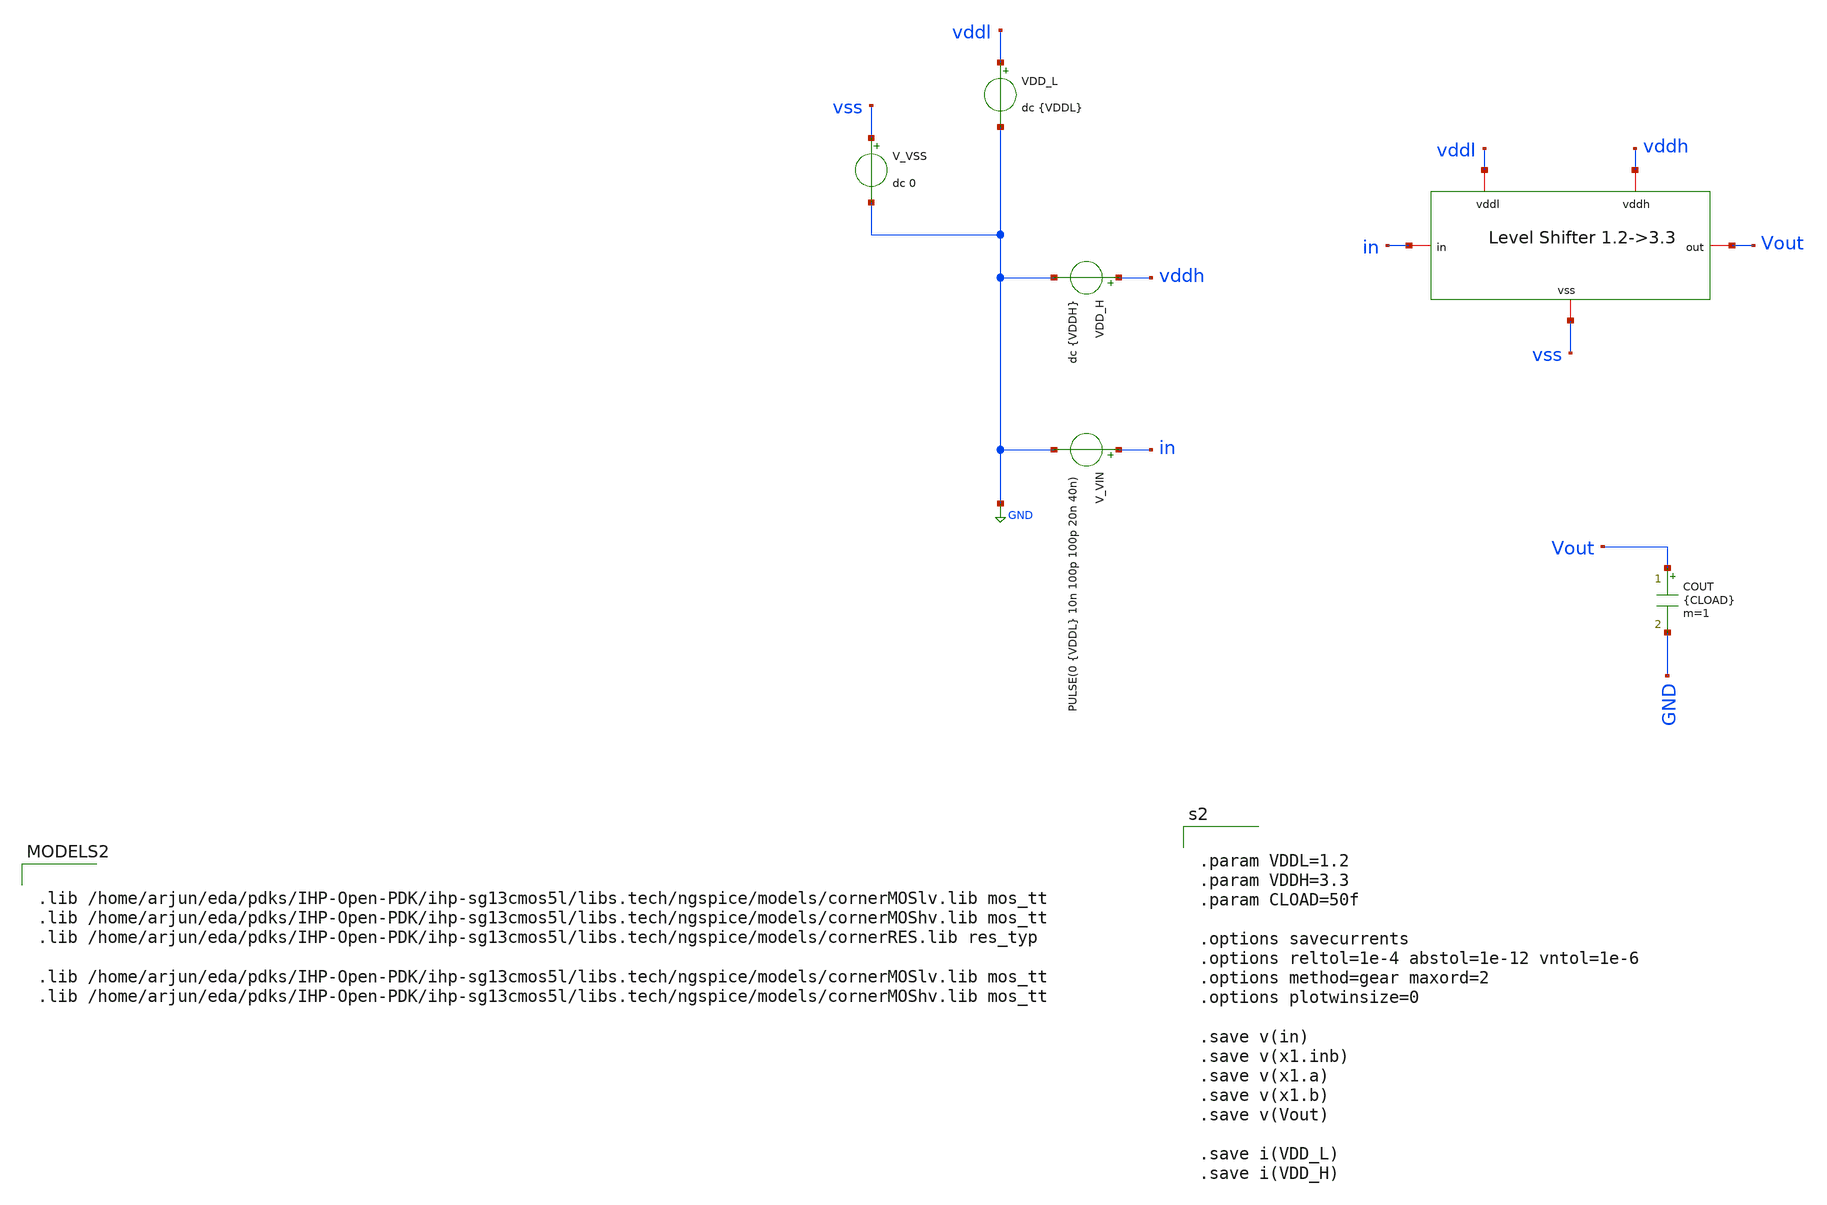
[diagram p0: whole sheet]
** sch_path: circuit_files/sar_adc_test/xschem/untitled-1.sch
**.subckt untitled-1
x1 vss vddl vddh Vout in level_shifter_1v2_to_3v3
V_VIN in GND PULSE(0 {VDDL} 10n 100p 100p 20n 40n)
VDD_L vddl GND dc {VDDL}
VDD_H vddh GND dc {VDDH}
V_VSS vss GND dc 0
COUT Vout GND {CLOAD} m=1
**** begin user architecture code

.lib /home/arjun/eda/pdks/IHP-Open-PDK/ihp-sg13cmos5l/libs.tech/ngspice/models/cornerMOSlv.lib mos_tt
.lib /home/arjun/eda/pdks/IHP-Open-PDK/ihp-sg13cmos5l/libs.tech/ngspice/models/cornerMOShv.lib mos_tt
.lib /home/arjun/eda/pdks/IHP-Open-PDK/ihp-sg13cmos5l/libs.tech/ngspice/models/cornerRES.lib res_typ

.lib /home/arjun/eda/pdks/IHP-Open-PDK/ihp-sg13cmos5l/libs.tech/ngspice/models/cornerMOSlv.lib mos_tt
.lib /home/arjun/eda/pdks/IHP-Open-PDK/ihp-sg13cmos5l/libs.tech/ngspice/models/cornerMOShv.lib mos_tt




.param VDDL=1.2
.param VDDH=3.3
.param CLOAD=50f

.options savecurrents
.options reltol=1e-4 abstol=1e-12 vntol=1e-6
.options method=gear maxord=2
.options plotwinsize=0

.save v(in)
.save v(x1.inb)
.save v(x1.a)
.save v(x1.b)
.save v(Vout)

.save i(VDD_L)
.save i(VDD_H)




.control

set noaskquit
set filetype=binary
set wr_singlescale
set wr_vecnames

* ============================================================
* CLEAN OLD RESULT FILES
* ============================================================

shell rm -f level_shifter_results.txt
shell rm -f level_shifter_nominal.txt
shell rm -f level_shifter_nominal.raw
shell rm -f level_shifter_load_sweep.txt
shell rm -f level_shifter_vddl_sweep.txt
shell rm -f level_shifter_vddh_sweep.txt


* ============================================================
* RESULT FILE HEADER
* ============================================================

echo ============================================================= > level_shifter_results.txt
echo IHP SG13CMOS5L 1.2V-to-3.3V Level Shifter Qualification >> level_shifter_results.txt
echo ============================================================= >> level_shifter_results.txt
echo . >> level_shifter_results.txt
echo Nominal VDDL  = 1.2 V >> level_shifter_results.txt
echo Nominal VDDH  = 3.3 V >> level_shifter_results.txt
echo Nominal CLOAD = 50 fF >> level_shifter_results.txt
echo . >> level_shifter_results.txt


* ============================================================
* 1. NOMINAL TRANSIENT
*
* Expected input source:
*
* V_VIN in 0 PULSE(0 {VDDL} 10n 100p 100p 20n 40n)
*
* RISE 1 = 10 ns
* FALL 1 = 30 ns
* RISE 2 = 50 ns
* FALL 2 = 70 ns
* ============================================================

alterparam VDDL=1.2
alterparam VDDH=3.3
alterparam CLOAD=50f

reset

tran 10p 90n


* ============================================================
* SAVE NOMINAL RAW FILE
* ============================================================

write level_shifter_nominal.raw


* ============================================================
* 2. NOMINAL STATIC LOGIC LEVELS
*
* t = 25 ns -> input HIGH
* t = 45 ns -> input LOW
* ============================================================

meas tran in_hi   FIND v(in)     AT=25n
meas tran inb_lo  FIND v(x1.inb) AT=25n
meas tran a_lo    FIND v(x1.a)   AT=25n
meas tran b_hi    FIND v(x1.b)   AT=25n
meas tran out_hi  FIND v(Vout)   AT=25n

meas tran in_lo   FIND v(in)     AT=45n
meas tran inb_hi  FIND v(x1.inb) AT=45n
meas tran a_hi    FIND v(x1.a)   AT=45n
meas tran b_lo    FIND v(x1.b)   AT=45n
meas tran out_lo  FIND v(Vout)   AT=45n


* ============================================================
* 3. PROPAGATION DELAY
*
* Use second complete cycle to avoid startup-state effects.
*
* Input 50%:
*     1.2 / 2 = 0.6 V
*
* Output 50%:
*     3.3 / 2 = 1.65 V
* ============================================================

meas tran tplh TRIG v(in) VAL=0.6 RISE=2 TARG v(Vout) VAL=1.65 RISE=2

meas tran tphl TRIG v(in) VAL=0.6 FALL=2 TARG v(Vout) VAL=1.65 FALL=2


* ============================================================
* 4. OUTPUT RISE/FALL TIME
*
* 10% VDDH = 0.33 V
* 90% VDDH = 2.97 V
* ============================================================

meas tran tr_out TRIG v(Vout) VAL=0.33 RISE=2 TARG v(Vout) VAL=2.97 RISE=2

meas tran tf_out TRIG v(Vout) VAL=2.97 FALL=2 TARG v(Vout) VAL=0.33 FALL=2


* ============================================================
* 5. INPUT INVERTER RISE/FALL
*
* Useful for determining whether the LV inverter itself
* becomes the speed bottleneck.
* ============================================================

meas tran tr_inb TRIG v(x1.inb) VAL=0.12 RISE=2 TARG v(x1.inb) VAL=1.08 RISE=2

meas tran tf_inb TRIG v(x1.inb) VAL=1.08 FALL=2 TARG v(x1.inb) VAL=0.12 FALL=2


* ============================================================
* 6. INTERNAL LEVEL-SHIFTER REGENERATION DELAY
*
* Measure how quickly A/B switch after input transition.
* ============================================================

meas tran t_in_rise WHEN v(in)=0.6 RISE=2
meas tran t_a_fall WHEN v(x1.a)=1.65 FALL=2
let t_regen_rise = t_a_fall - t_in_rise

meas tran t_in_fall WHEN v(in)=0.6 FALL=2
meas tran t_a_rise WHEN v(x1.a)=1.65 RISE=2
let t_regen_fall = t_a_rise - t_in_fall


* ============================================================
* 7. AVERAGE POWER
*
* Measure over two complete 40-ns input periods:
* 10 ns -> 90 ns
* ============================================================

meas tran iddl_avg AVG i(VDD_L) FROM=10n TO=90n
meas tran iddh_avg AVG i(VDD_H) FROM=10n TO=90n

let pavg_vddl = -1.2*iddl_avg
let pavg_vddh = -3.3*iddh_avg
let pavg_total = pavg_vddl + pavg_vddh

* Energy associated with one full 40 ns HIGH+LOW input cycle
let energy_cycle = pavg_total*40n


* ============================================================
* 8. STATIC POWER - INPUT HIGH
*
* Input is stable HIGH between ~10.1 and 30 ns.
* Use 20-28 ns, well away from edges.
* ============================================================

meas tran iddl_static_hi AVG i(VDD_L) FROM=20n TO=28n
meas tran iddh_static_hi AVG i(VDD_H) FROM=20n TO=28n

let pstatic_hi_l = -1.2*iddl_static_hi
let pstatic_hi_h = -3.3*iddh_static_hi
let pstatic_hi = pstatic_hi_l + pstatic_hi_h


* ============================================================
* 9. STATIC POWER - INPUT LOW
*
* Input is stable LOW from ~30.1 to 50 ns.
* ============================================================

meas tran iddl_static_lo AVG i(VDD_L) FROM=40n TO=48n
meas tran iddh_static_lo AVG i(VDD_H) FROM=40n TO=48n

let pstatic_lo_l = -1.2*iddl_static_lo
let pstatic_lo_h = -3.3*iddh_static_lo
let pstatic_lo = pstatic_lo_l + pstatic_lo_h


* ============================================================
* 10. NOMINAL FUNCTIONAL PASS CHECK
*
* Requirements:
*
* OUT HIGH > 90% VDDH = 2.97 V
* OUT LOW  < 10% VDDH = 0.33 V
*
* Internal A/B nodes must also resolve correctly.
* ============================================================

let functional_pass = 0

if out_hi > 2.97
  if out_lo < 0.33
    if a_lo < 0.33
      if a_hi > 2.97
        if b_hi > 2.97
          if b_lo < 0.33
            let functional_pass = 1
          end
        end
      end
    end
  end
end


* ============================================================
* 11. WRITE NOMINAL RESULTS
* ============================================================

echo ------------------------------------------------------------- >> level_shifter_results.txt
echo NOMINAL LOGIC LEVELS >> level_shifter_results.txt
echo ------------------------------------------------------------- >> level_shifter_results.txt

echo IN_high          = $&in_hi V >> level_shifter_results.txt
echo INB_low          = $&inb_lo V >> level_shifter_results.txt
echo A_low            = $&a_lo V >> level_shifter_results.txt
echo B_high           = $&b_hi V >> level_shifter_results.txt
echo OUT_high         = $&out_hi V >> level_shifter_results.txt

echo . >> level_shifter_results.txt

echo IN_low           = $&in_lo V >> level_shifter_results.txt
echo INB_high         = $&inb_hi V >> level_shifter_results.txt
echo A_high           = $&a_hi V >> level_shifter_results.txt
echo B_low            = $&b_lo V >> level_shifter_results.txt
echo OUT_low          = $&out_lo V >> level_shifter_results.txt

echo . >> level_shifter_results.txt


echo ------------------------------------------------------------- >> level_shifter_results.txt
echo TIMING >> level_shifter_results.txt
echo ------------------------------------------------------------- >> level_shifter_results.txt

echo TPLH             = $&tplh s >> level_shifter_results.txt
echo TPHL             = $&tphl s >> level_shifter_results.txt
echo OUT_rise_10_90   = $&tr_out s >> level_shifter_results.txt
echo OUT_fall_90_10   = $&tf_out s >> level_shifter_results.txt
echo INB_rise_10_90   = $&tr_inb s >> level_shifter_results.txt
echo INB_fall_90_10   = $&tf_inb s >> level_shifter_results.txt
echo Regen_input_rise = $&t_regen_rise s >> level_shifter_results.txt
echo Regen_input_fall = $&t_regen_fall s >> level_shifter_results.txt

echo . >> level_shifter_results.txt


echo ------------------------------------------------------------- >> level_shifter_results.txt
echo POWER >> level_shifter_results.txt
echo ------------------------------------------------------------- >> level_shifter_results.txt

echo IDDL_average      = $&iddl_avg A >> level_shifter_results.txt
echo IDDH_average      = $&iddh_avg A >> level_shifter_results.txt

echo Pavg_VDDL         = $&pavg_vddl W >> level_shifter_results.txt
echo Pavg_VDDH         = $&pavg_vddh W >> level_shifter_results.txt
echo Pavg_total        = $&pavg_total W >> level_shifter_results.txt

echo Energy_per_cycle  = $&energy_cycle J >> level_shifter_results.txt

echo . >> level_shifter_results.txt

echo Pstatic_IN_HIGH   = $&pstatic_hi W >> level_shifter_results.txt
echo Pstatic_IN_LOW    = $&pstatic_lo W >> level_shifter_results.txt

echo . >> level_shifter_results.txt


echo ------------------------------------------------------------- >> level_shifter_results.txt
echo FUNCTIONAL RESULT >> level_shifter_results.txt
echo ------------------------------------------------------------- >> level_shifter_results.txt

echo FUNCTIONAL_PASS   = $&functional_pass >> level_shifter_results.txt

echo . >> level_shifter_results.txt


* ============================================================
* 12. SAVE NOMINAL ASCII WAVEFORM
* ============================================================

wrdata level_shifter_nominal.txt v(in) v(x1.inb) v(x1.a) v(x1.b) v(Vout)


* ============================================================
* 13. OUTPUT LOAD SWEEP
*
* Tests whether the output buffer can drive increasingly
* heavy gate/capacitive loads.
* ============================================================

echo ============================================================= > level_shifter_load_sweep.txt
echo IHP SG13CMOS5L LEVEL SHIFTER OUTPUT LOAD SWEEP >> level_shifter_load_sweep.txt
echo VDDL=1.2V VDDH=3.3V >> level_shifter_load_sweep.txt
echo Columns: CLOAD TPLH TPHL TRISE TFALL OUT_HIGH OUT_LOW PAVG ENERGY PASS >>
+ level_shifter_load_sweep.txt
echo ============================================================= >> level_shifter_load_sweep.txt

foreach cl 20f 50f 100f 200f 500f 1p

  alterparam VDDL=1.2
  alterparam VDDH=3.3
  alterparam CLOAD=$cl

  reset

  tran 10p 90n

  meas tran d_lh TRIG v(in) VAL=0.6 RISE=2 TARG v(Vout) VAL=1.65 RISE=2

  meas tran d_hl TRIG v(in) VAL=0.6 FALL=2 TARG v(Vout) VAL=1.65 FALL=2

  meas tran rtime TRIG v(Vout) VAL=0.33 RISE=2 TARG v(Vout) VAL=2.97 RISE=2

  meas tran ftime TRIG v(Vout) VAL=2.97 FALL=2 TARG v(Vout) VAL=0.33 FALL=2

  meas tran oh FIND v(Vout) AT=25n
  meas tran ol FIND v(Vout) AT=45n

  meas tran il AVG i(VDD_L) FROM=10n TO=90n
  meas tran ih AVG i(VDD_H) FROM=10n TO=90n

  let p_l = -1.2*il
  let p_h = -3.3*ih
  let p_total = p_l + p_h
  let e_toggle = p_total*40n

  let pass_load = 0

  if oh > 2.97
    if ol < 0.33
      let pass_load = 1
    end
  end

  echo $cl $&d_lh $&d_hl $&rtime $&ftime $&oh $&ol $&p_total $&e_toggle $&pass_load >>
+ level_shifter_load_sweep.txt

end


* ============================================================
* 14. VDDL SWEEP
*
* Characterize low-voltage digital supply variation.
*
* Nominal standard-cell domain:
*       1.20 V
*
* Test:
*       1.08 -> 1.32 V
* ============================================================

echo ============================================================= > level_shifter_vddl_sweep.txt
echo IHP SG13CMOS5L LEVEL SHIFTER VDDL SWEEP >> level_shifter_vddl_sweep.txt
echo VDDH=3.3V CLOAD=50f >> level_shifter_vddl_sweep.txt
echo Columns: VDDL TPLH TPHL OUT_HIGH OUT_LOW A_LOW A_HIGH B_HIGH B_LOW PASS >>
+ level_shifter_vddl_sweep.txt
echo ============================================================= >> level_shifter_vddl_sweep.txt

foreach vl 1.08 1.14 1.20 1.26 1.32

  alterparam VDDL=$vl
  alterparam VDDH=3.3
  alterparam CLOAD=50f

  reset

  tran 10p 90n

  let vl50 = 0.5*$vl

  meas tran d_lh TRIG v(in) VAL=$&vl50 RISE=2 TARG v(Vout) VAL=1.65 RISE=2

  meas tran d_hl TRIG v(in) VAL=$&vl50 FALL=2 TARG v(Vout) VAL=1.65 FALL=2

  meas tran oh FIND v(Vout) AT=25n
  meas tran ol FIND v(Vout) AT=45n

  meas tran al FIND v(x1.a) AT=25n
  meas tran ah FIND v(x1.a) AT=45n

  meas tran bh FIND v(x1.b) AT=25n
  meas tran bl FIND v(x1.b) AT=45n

  let pass_vl = 0

  if oh > 2.97
    if ol < 0.33
      if al < 0.33
        if ah > 2.97
          if bh > 2.97
            if bl < 0.33
              let pass_vl = 1
            end
          end
        end
      end
    end
  end

  echo $vl $&d_lh $&d_hl $&oh $&ol $&al $&ah $&bh $&bl $&pass_vl >> level_shifter_vddl_sweep.txt

end


* ============================================================
* 15. VDDH SWEEP
*
* Characterize HV-domain supply range.
* ============================================================

echo ============================================================= > level_shifter_vddh_sweep.txt
echo IHP SG13CMOS5L LEVEL SHIFTER VDDH SWEEP >> level_shifter_vddh_sweep.txt
echo VDDL=1.2V CLOAD=50f >> level_shifter_vddh_sweep.txt
echo Columns: VDDH TPLH TPHL OUT_HIGH OUT_LOW PAVG PASS >> level_shifter_vddh_sweep.txt
echo ============================================================= >> level_shifter_vddh_sweep.txt

foreach vh 3.0 3.15 3.3 3.45 3.6

  alterparam VDDL=1.2
  alterparam VDDH=$vh
  alterparam CLOAD=50f

  reset

  tran 10p 90n

  let vh50 = 0.5*$vh
  let vh90 = 0.9*$vh
  let vh10 = 0.1*$vh

  meas tran d_lh TRIG v(in) VAL=0.6 RISE=2 TARG v(Vout) VAL=$&vh50 RISE=2

  meas tran d_hl TRIG v(in) VAL=0.6 FALL=2 TARG v(Vout) VAL=$&vh50 FALL=2

  meas tran oh FIND v(Vout) AT=25n
  meas tran ol FIND v(Vout) AT=45n

  meas tran il AVG i(VDD_L) FROM=10n TO=90n
  meas tran ih AVG i(VDD_H) FROM=10n TO=90n

  let p_l = -1.2*il
  let p_h = -$vh*ih
  let p_total = p_l + p_h

  let pass_vh = 0

  if oh > vh90
    if ol < vh10
      let pass_vh = 1
    end
  end

  echo $vh $&d_lh $&d_hl $&oh $&ol $&p_total $&pass_vh >> level_shifter_vddh_sweep.txt

end


* ============================================================
* 16. RESTORE NOMINAL CONDITIONS FOR FINAL PLOTS
* ============================================================

alterparam VDDL=1.2
alterparam VDDH=3.3
alterparam CLOAD=50f

reset

tran 10p 90n


* ============================================================
* 17. SHOW PLOTS
* ============================================================

plot v(in) v(x1.inb) title '1.2-V Input and Complement'

plot v(x1.a) v(x1.b) v(Vout) title '3.3-V Level-Shifter Core and Output'


* ============================================================
* 18. FINAL CONSOLE SUMMARY
* ============================================================

echo .
echo =============================================================
echo LEVEL SHIFTER QUALIFICATION COMPLETE
echo =============================================================
echo .
echo Nominal qualification:
echo   level_shifter_results.txt
echo .
echo Nominal waveform data:
echo   level_shifter_nominal.txt
echo   level_shifter_nominal.raw
echo .
echo Output-load sweep:
echo   level_shifter_load_sweep.txt
echo .
echo Low-voltage supply sweep:
echo   level_shifter_vddl_sweep.txt
echo .
echo High-voltage supply sweep:
echo   level_shifter_vddh_sweep.txt
echo .
echo =============================================================

.endc


**** end user architecture code
**.ends

* expanding   symbol:  level_shifter_1v2_to_3v3.sym # of pins=5
** sym_path: circuit_files/sar_adc_test/xschem/level_shifter_1v2_to_3v3.sym
** sch_path: circuit_files/sar_adc_test/xschem/level_shifter_1v2_to_3v3.sch
.subckt level_shifter_1v2_to_3v3 vss vddl vddh out in
*.iopin vddl
*.iopin vddh
*.iopin out
*.iopin vss
*.iopin in
XM1 inb in vss vss sg13_lv_nmos w=0.6u l=0.13u ng=1 m=1 mm_ok=1
XM2 inb in vddl vddl sg13_lv_pmos w=1.2u l=0.13u ng=1 m=1 mm_ok=1
XM3 a in vss vss sg13_hv_nmos w=2u l=0.45u ng=1 m=4 mm_ok=1
XM4 b inb vss vss sg13_hv_nmos w=2u l=0.45u ng=1 m=4 mm_ok=1
XM5 b a vddh vddh sg13_hv_pmos w=2u l=0.4u ng=1 m=1 mm_ok=1
XM6 a b vddh vddh sg13_hv_pmos w=2u l=0.4u ng=1 m=1 mm_ok=1
XM12 out a vss vss sg13_hv_nmos w=2u l=0.45u ng=1 m=1 mm_ok=1
XM16 out a vddh vddh sg13_hv_pmos w=2u l=0.4u ng=1 m=2 mm_ok=1
.ends

.GLOBAL GND
.end
